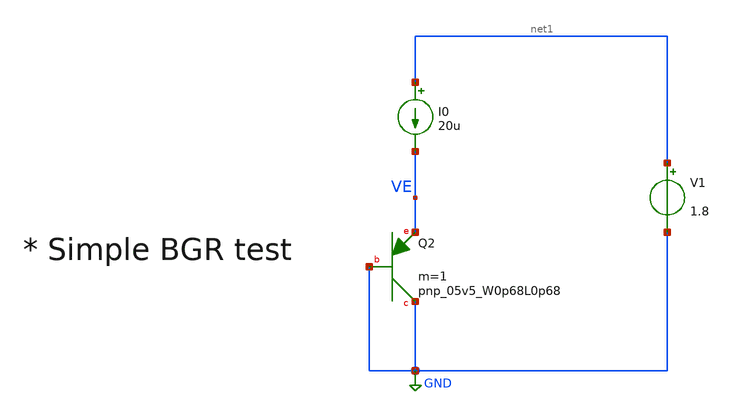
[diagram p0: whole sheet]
** sch_path: design/bgr/CTAT.sch
**.subckt CTAT
I0 net1 VE 20u
V1 net1 GND 1.8
XQ2 GND GND VE sky130_fd_pr__pnp_05v5_W0p68L0p68 m=1
**** begin user architecture code


.param temp=27

.dc temp -40 125 1


.save all




.options wnflag=1
.include $::SKYWATER_MODELS/cells/nfet_01v8/sky130_fd_pr__nfet_01v8__tt.corner.spice
.include $::SKYWATER_MODELS/cells/nfet_01v8_lvt/sky130_fd_pr__nfet_01v8_lvt__tt.corner.spice
.include $::SKYWATER_MODELS/cells/pfet_01v8/sky130_fd_pr__pfet_01v8__tt.corner.spice
.include $::SKYWATER_MODELS/cells/nfet_03v3_nvt/sky130_fd_pr__nfet_03v3_nvt__tt.corner.spice
.include $::SKYWATER_MODELS/cells/nfet_05v0_nvt/sky130_fd_pr__nfet_05v0_nvt__tt.corner.spice
.include $::SKYWATER_MODELS/cells/esd_nfet_01v8/sky130_fd_pr__esd_nfet_01v8__tt.corner.spice
.include $::SKYWATER_MODELS/cells/pfet_01v8_lvt/sky130_fd_pr__pfet_01v8_lvt__tt.corner.spice
.include $::SKYWATER_MODELS/cells/pfet_01v8_hvt/sky130_fd_pr__pfet_01v8_hvt__tt.corner.spice
.include $::SKYWATER_MODELS/cells/esd_pfet_g5v0d10v5/sky130_fd_pr__esd_pfet_g5v0d10v5__tt.corner.spice
.include $::SKYWATER_MODELS/cells/pfet_g5v0d10v5/sky130_fd_pr__pfet_g5v0d10v5__tt.corner.spice
.include $::SKYWATER_MODELS/cells/pfet_g5v0d16v0/sky130_fd_pr__pfet_g5v0d16v0__tt.corner.spice
.include $::SKYWATER_MODELS/cells/nfet_g5v0d10v5/sky130_fd_pr__nfet_g5v0d10v5__tt.corner.spice
.include $::SKYWATER_MODELS/cells/nfet_g5v0d16v0/sky130_fd_pr__nfet_g5v0d16v0__tt_discrete.corner.spice
.include $::SKYWATER_MODELS/cells/esd_nfet_g5v0d10v5/sky130_fd_pr__esd_nfet_g5v0d10v5__tt.corner.spice
.include $::SKYWATER_MODELS/cells/pnp_05v5/sky130_fd_pr__pnp_05v5_W0p68L0p68.model.spice


.include $::SKYWATER_MODELS/models/corners/tt/nonfet.spice



* Mismatch parameters
.include $::SKYWATER_MODELS/cells/nfet_01v8/sky130_fd_pr__nfet_01v8__mismatch.corner.spice
.include $::SKYWATER_MODELS/cells/pfet_01v8/sky130_fd_pr__pfet_01v8__mismatch.corner.spice
.include $::SKYWATER_MODELS/cells/nfet_01v8_lvt/sky130_fd_pr__nfet_01v8_lvt__mismatch.corner.spice
.include $::SKYWATER_MODELS/cells/pfet_01v8_lvt/sky130_fd_pr__pfet_01v8_lvt__mismatch.corner.spice
.include $::SKYWATER_MODELS/cells/pfet_01v8_hvt/sky130_fd_pr__pfet_01v8_hvt__mismatch.corner.spice
.include $::SKYWATER_MODELS/cells/nfet_g5v0d10v5/sky130_fd_pr__nfet_g5v0d10v5__mismatch.corner.spice
.include $::SKYWATER_MODELS/cells/pfet_g5v0d10v5/sky130_fd_pr__pfet_g5v0d10v5__mismatch.corner.spice
.include $::SKYWATER_MODELS/cells/nfet_05v0_nvt/sky130_fd_pr__nfet_05v0_nvt__mismatch.corner.spice
.include $::SKYWATER_MODELS/cells/nfet_03v3_nvt/sky130_fd_pr__nfet_03v3_nvt__mismatch.corner.spice
* Resistor$::SKYWATER_MODELS/Capacitor
.include $::SKYWATER_MODELS/models/r+c/res_typical__cap_typical.spice
.include $::SKYWATER_MODELS/models/r+c/res_typical__cap_typical__lin.spice
* Special cells
.include $::SKYWATER_MODELS/models/corners/tt/specialized_cells.spice
* All models
.include $::SKYWATER_MODELS/models/all.spice
* Corner
.include $::SKYWATER_MODELS/models/corners/tt/rf.spice

**** end user architecture code
**.ends
.GLOBAL GND
.end
